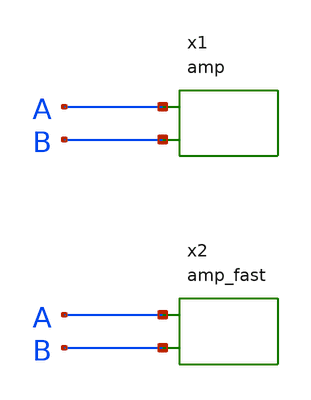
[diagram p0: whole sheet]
** sch_path: tests/golden/SCHEM/cases/SCHEM-NL-15/input/nl15.sch
**.subckt nl15
x1 A B amp
x2 A B amp_fast
**.ends

* expanding   symbol:  amp.sym # of pins=2
** sym_path: tests/golden/SCHEM/cases/SCHEM-NL-15/input/amp.sym
** sch_path: tests/golden/SCHEM/cases/SCHEM-NL-15/input/amp.sch
.subckt amp IN OUT
*.iopin IN
*.iopin OUT
R1 IN OUT 1k m=1
.ends


* expanding   symbol:  amp_fast.sym # of pins=2
** sym_path: tests/golden/SCHEM/cases/SCHEM-NL-15/input/amp.sym
** sch_path: tests/golden/SCHEM/cases/SCHEM-NL-15/input/amp_fast.sch
.subckt amp_fast IN OUT
*.iopin IN
*.iopin OUT
R1 IN OUT 100 m=1
.ends

.end
